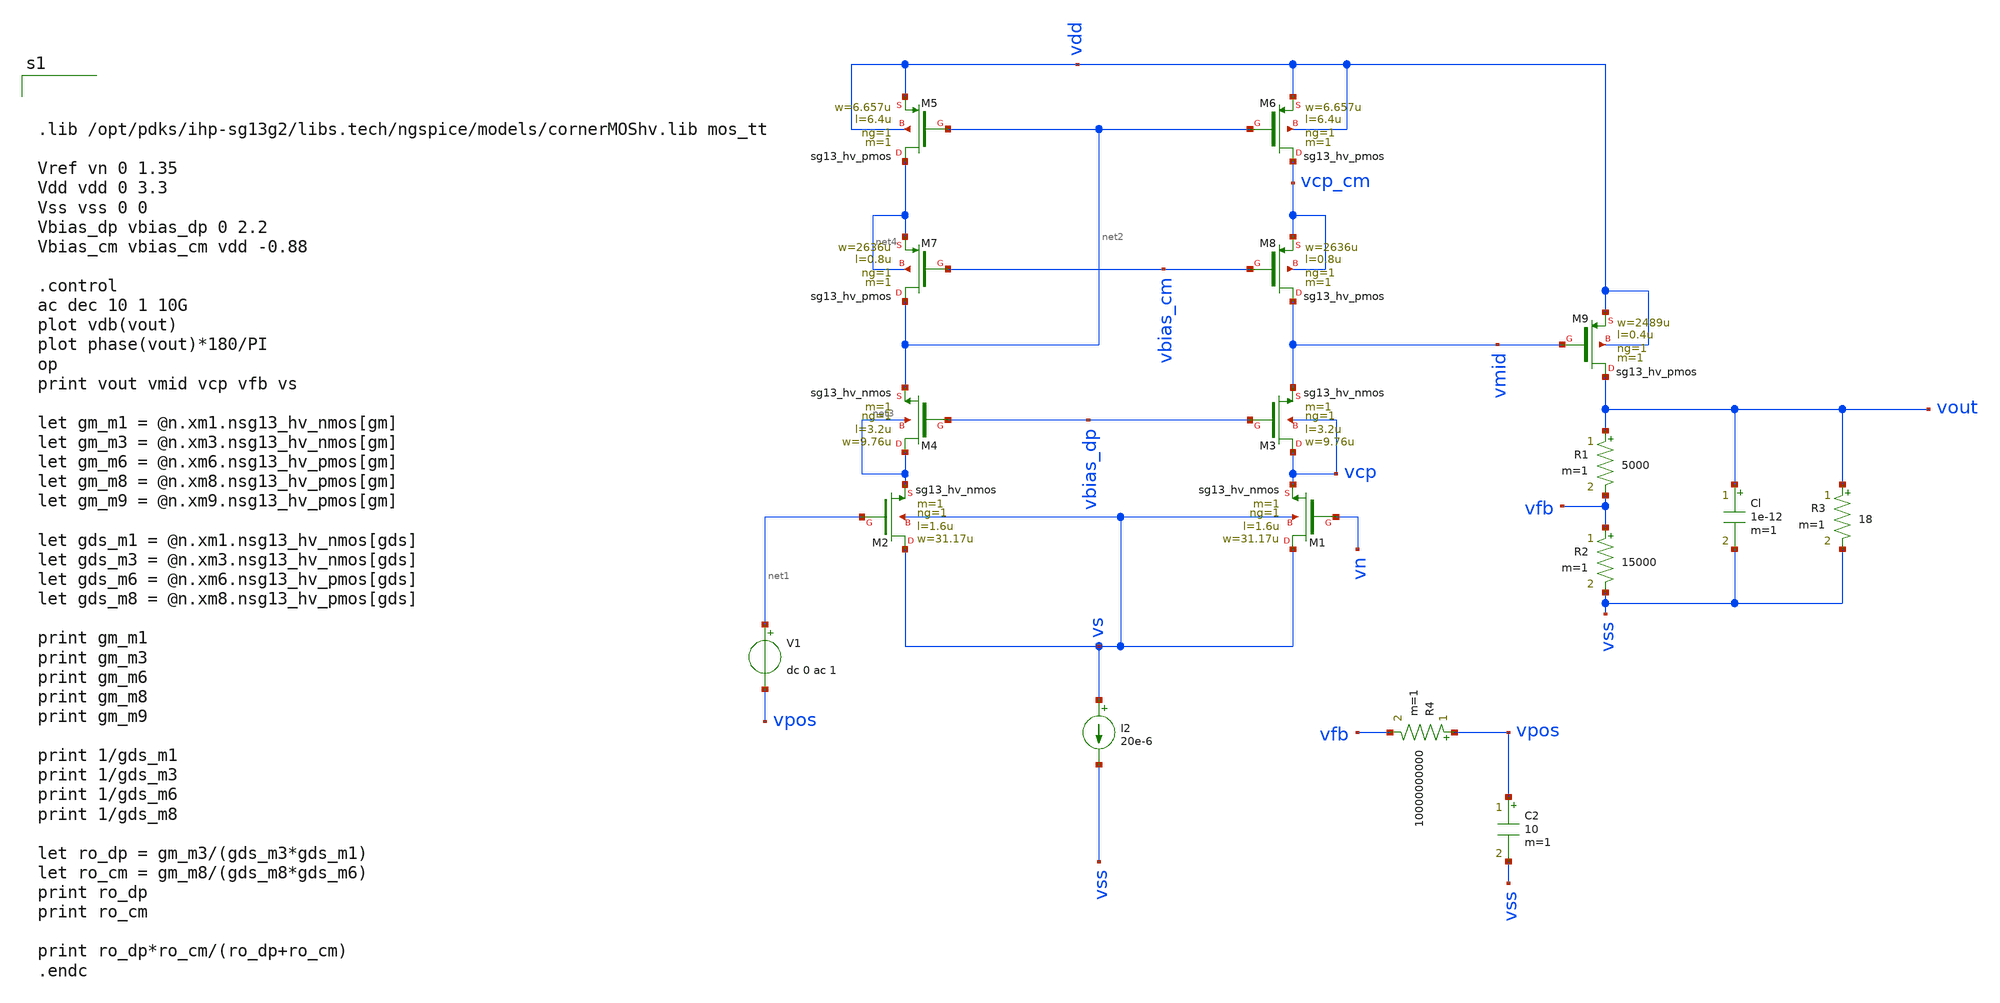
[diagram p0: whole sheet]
** sch_path: test/Tesis_notebooks/xschem/ldo_ol_sim_ihp_cc_full.sch
**.subckt ldo_ol_sim_ihp_cc_full
R1 vout vfb 5000 m=1
R2 vfb vss 15000 m=1
Cl vout vss 1e-12 m=1
XM7 net2 vbias_cm net4 net4 sg13_hv_pmos w=2636u l=0.8u ng=1 m=1 mm_ok=1
I2 vs vss 20e-6
XM1 vs vn vcp vs sg13_hv_nmos w=31.17u l=1.6u ng=1 m=1 mm_ok=1
XM2 vs net1 net3 vs sg13_hv_nmos w=31.17u l=1.6u ng=1 m=1 mm_ok=1
XM3 vcp vbias_dp vmid vcp sg13_hv_nmos w=9.76u l=3.2u ng=1 m=1 mm_ok=1
XM4 net3 vbias_dp net2 net3 sg13_hv_nmos w=9.76u l=3.2u ng=1 m=1 mm_ok=1
XM5 net4 net2 vdd vdd sg13_hv_pmos w=6.657u l=6.4u ng=1 m=1 mm_ok=1
XM6 vcp_cm net2 vdd vdd sg13_hv_pmos w=6.657u l=6.4u ng=1 m=1 mm_ok=1
XM8 vmid vbias_cm vcp_cm vcp_cm sg13_hv_pmos w=2636u l=0.8u ng=1 m=1 mm_ok=1
XM9 vout vmid vdd vdd sg13_hv_pmos w=2489u l=0.4u ng=1 m=1 mm_ok=1
R4 vpos vfb 10000000000 m=1
C2 vpos vss 10 m=1
V1 net1 vpos dc 0 ac 1
R3 vout vss 18 m=1
**** begin user architecture code



.lib /opt/pdks/ihp-sg13g2/libs.tech/ngspice/models/cornerMOShv.lib mos_tt

Vref vn 0 1.35
Vdd vdd 0 3.3
Vss vss 0 0
Vbias_dp vbias_dp 0 2.2
Vbias_cm vbias_cm vdd -0.88

.control
ac dec 10 1 10G
plot vdb(vout)
plot phase(vout)*180/PI
op
print vout vmid vcp vfb vs

let gm_m1 = @n.xm1.nsg13_hv_nmos[gm]
let gm_m3 = @n.xm3.nsg13_hv_nmos[gm]
let gm_m6 = @n.xm6.nsg13_hv_pmos[gm]
let gm_m8 = @n.xm8.nsg13_hv_pmos[gm]
let gm_m9 = @n.xm9.nsg13_hv_pmos[gm]

let gds_m1 = @n.xm1.nsg13_hv_nmos[gds]
let gds_m3 = @n.xm3.nsg13_hv_nmos[gds]
let gds_m6 = @n.xm6.nsg13_hv_pmos[gds]
let gds_m8 = @n.xm8.nsg13_hv_pmos[gds]

print gm_m1
print gm_m3
print gm_m6
print gm_m8
print gm_m9

print 1/gds_m1
print 1/gds_m3
print 1/gds_m6
print 1/gds_m8

let ro_dp = gm_m3/(gds_m3*gds_m1)
let ro_cm = gm_m8/(gds_m8*gds_m6)
print ro_dp
print ro_cm

print ro_dp*ro_cm/(ro_dp+ro_cm)
.endc



**** end user architecture code
**.ends
.end
